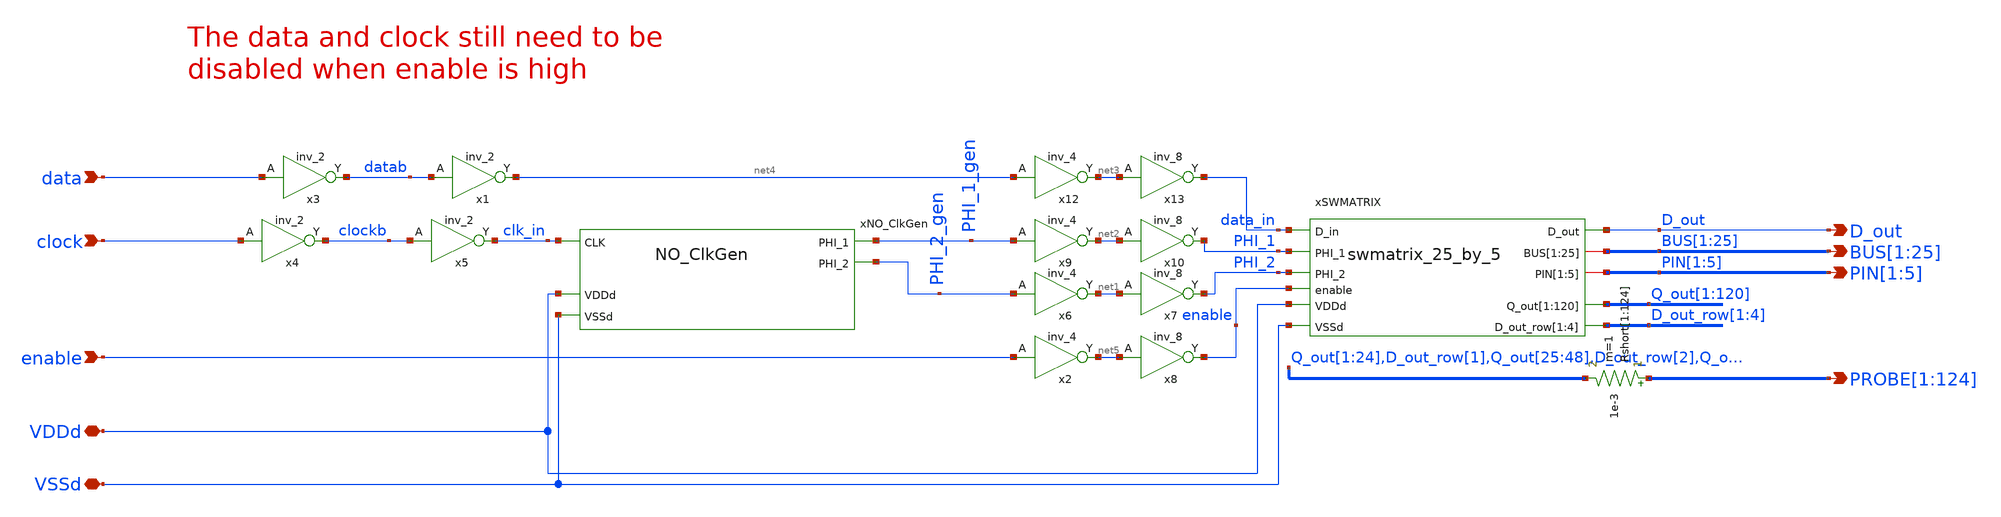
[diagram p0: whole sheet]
** sch_path: full_switch_matrix_25_by_5/full_switch_matrix_25_by_5.sch
**.subckt full_switch_matrix_25_by_5 data clock enable D_out PIN[1],PIN[2],PIN[3],PIN[4],PIN[5]
*+ BUS[1],BUS[2],BUS[3],BUS[4],BUS[5],BUS[6],BUS[7],BUS[8],BUS[9],BUS[10],BUS[11],BUS[12],BUS[13],BUS[14],BUS[15],BUS[16],BUS[17],BUS[18],BUS[19],BUS[20],BUS[21],BUS[22],BUS[23],BUS[24],BUS[25] VSSd VDDd
*+ PROBE[1],PROBE[2],PROBE[3],PROBE[4],PROBE[5],PROBE[6],PROBE[7],PROBE[8],PROBE[9],PROBE[10],PROBE[11],PROBE[12],PROBE[13],PROBE[14],PROBE[15],PROBE[16],PROBE[17],PROBE[18],PROBE[19],PROBE[20],PROBE[21],PROBE[22],PROBE[23],PROBE[24],PROBE[25],PROBE[26],PROBE[27],PROBE[28],PROBE[29],PROBE[30],PROBE[31],PROBE[32],PROBE[33],PROBE[34],PROBE[35],PROBE[36],PROBE[37],PROBE[38],PROBE[39],PROBE[40],PROBE[41],PROBE[42],PROBE[43],PROBE[44],PROBE[45],PROBE[46],PROBE[47],PROBE[48],PROBE[49],PROBE[50],PROBE[51],PROBE[52],PROBE[53],PROBE[54],PROBE[55],PROBE[56],PROBE[57],PROBE[58],PROBE[59],PROBE[60],PROBE[61],PROBE[62],PROBE[63],PROBE[64],PROBE[65],PROBE[66],PROBE[67],PROBE[68],PROBE[69],PROBE[70],PROBE[71],PROBE[72],PROBE[73],PROBE[74],PROBE[75],PROBE[76],PROBE[77],PROBE[78],PROBE[79],PROBE[80],PROBE[81],PROBE[82],PROBE[83],PROBE[84],PROBE[85],PROBE[86],PROBE[87],PROBE[88],PROBE[89],PROBE[90],PROBE[91],PROBE[92],PROBE[93],PROBE[94],PROBE[95],PROBE[96],PROBE[97],PROBE[98],PROBE[99],PROBE[100],PROBE[101],PROBE[102],PROBE[103],PROBE[104],PROBE[105],PROBE[106],PROBE[107],PROBE[108],PROBE[109],PROBE[110],PROBE[111],PROBE[112],PROBE[113],PROBE[114],PROBE[115],PROBE[116],PROBE[117],PROBE[118],PROBE[119],PROBE[120],PROBE[121],PROBE[122],PROBE[123],PROBE[124]
*.ipin data
*.ipin clock
*.ipin enable
*.opin D_out
*.opin PIN[1],PIN[2],PIN[3],PIN[4],PIN[5]
*.opin
*+ BUS[1],BUS[2],BUS[3],BUS[4],BUS[5],BUS[6],BUS[7],BUS[8],BUS[9],BUS[10],BUS[11],BUS[12],BUS[13],BUS[14],BUS[15],BUS[16],BUS[17],BUS[18],BUS[19],BUS[20],BUS[21],BUS[22],BUS[23],BUS[24],BUS[25]
*.iopin VSSd
*.iopin VDDd
*.opin
*+ PROBE[1],PROBE[2],PROBE[3],PROBE[4],PROBE[5],PROBE[6],PROBE[7],PROBE[8],PROBE[9],PROBE[10],PROBE[11],PROBE[12],PROBE[13],PROBE[14],PROBE[15],PROBE[16],PROBE[17],PROBE[18],PROBE[19],PROBE[20],PROBE[21],PROBE[22],PROBE[23],PROBE[24],PROBE[25],PROBE[26],PROBE[27],PROBE[28],PROBE[29],PROBE[30],PROBE[31],PROBE[32],PROBE[33],PROBE[34],PROBE[35],PROBE[36],PROBE[37],PROBE[38],PROBE[39],PROBE[40],PROBE[41],PROBE[42],PROBE[43],PROBE[44],PROBE[45],PROBE[46],PROBE[47],PROBE[48],PROBE[49],PROBE[50],PROBE[51],PROBE[52],PROBE[53],PROBE[54],PROBE[55],PROBE[56],PROBE[57],PROBE[58],PROBE[59],PROBE[60],PROBE[61],PROBE[62],PROBE[63],PROBE[64],PROBE[65],PROBE[66],PROBE[67],PROBE[68],PROBE[69],PROBE[70],PROBE[71],PROBE[72],PROBE[73],PROBE[74],PROBE[75],PROBE[76],PROBE[77],PROBE[78],PROBE[79],PROBE[80],PROBE[81],PROBE[82],PROBE[83],PROBE[84],PROBE[85],PROBE[86],PROBE[87],PROBE[88],PROBE[89],PROBE[90],PROBE[91],PROBE[92],PROBE[93],PROBE[94],PROBE[95],PROBE[96],PROBE[97],PROBE[98],PROBE[99],PROBE[100],PROBE[101],PROBE[102],PROBE[103],PROBE[104],PROBE[105],PROBE[106],PROBE[107],PROBE[108],PROBE[109],PROBE[110],PROBE[111],PROBE[112],PROBE[113],PROBE[114],PROBE[115],PROBE[116],PROBE[117],PROBE[118],PROBE[119],PROBE[120],PROBE[121],PROBE[122],PROBE[123],PROBE[124]
xNO_ClkGen PHI_2_gen clk_in PHI_1_gen VDDd VSSd NO_ClkGen
x3 data VSSd VDDd VSSd VDDd datab gf180mcu_fd_sc_mcu9t5v0__inv_2
x1 datab VSSd VDDd VSSd VDDd net4 gf180mcu_fd_sc_mcu9t5v0__inv_2
x4 clock VSSd VDDd VSSd VDDd clockb gf180mcu_fd_sc_mcu9t5v0__inv_2
x5 clockb VSSd VDDd VSSd VDDd clk_in gf180mcu_fd_sc_mcu9t5v0__inv_2
x6 PHI_2_gen VSSd VDDd VSSd VDDd net1 gf180mcu_fd_sc_mcu9t5v0__inv_4
x7 net1 VSSd VDDd VSSd VDDd PHI_2 gf180mcu_fd_sc_mcu9t5v0__inv_8
x9 PHI_1_gen VSSd VDDd VSSd VDDd net2 gf180mcu_fd_sc_mcu9t5v0__inv_4
x10 net2 VSSd VDDd VSSd VDDd PHI_1 gf180mcu_fd_sc_mcu9t5v0__inv_8
x12 net4 VSSd VDDd VSSd VDDd net3 gf180mcu_fd_sc_mcu9t5v0__inv_4
x13 net3 VSSd VDDd VSSd VDDd data_in gf180mcu_fd_sc_mcu9t5v0__inv_8
x2 enable VSSd VDDd VSSd VDDd net5 gf180mcu_fd_sc_mcu9t5v0__inv_4
x8 net5 VSSd VDDd VSSd VDDd enable gf180mcu_fd_sc_mcu9t5v0__inv_8
xSWMATRIX data_in D_out PHI_1 PHI_2 BUS[1] BUS[2] BUS[3] BUS[4] BUS[5] BUS[6] BUS[7] BUS[8] BUS[9]
+ BUS[10] BUS[11] BUS[12] BUS[13] BUS[14] BUS[15] BUS[16] BUS[17] BUS[18] BUS[19] BUS[20] BUS[21] BUS[22]
+ BUS[23] BUS[24] BUS[25] PIN[1] PIN[2] PIN[3] PIN[4] PIN[5] VDDd VSSd enable Q_out[1] Q_out[2] Q_out[3]
+ Q_out[4] Q_out[5] Q_out[6] Q_out[7] Q_out[8] Q_out[9] Q_out[10] Q_out[11] Q_out[12] Q_out[13] Q_out[14]
+ Q_out[15] Q_out[16] Q_out[17] Q_out[18] Q_out[19] Q_out[20] Q_out[21] Q_out[22] Q_out[23] Q_out[24] Q_out[25]
+ Q_out[26] Q_out[27] Q_out[28] Q_out[29] Q_out[30] Q_out[31] Q_out[32] Q_out[33] Q_out[34] Q_out[35] Q_out[36]
+ Q_out[37] Q_out[38] Q_out[39] Q_out[40] Q_out[41] Q_out[42] Q_out[43] Q_out[44] Q_out[45] Q_out[46] Q_out[47]
+ Q_out[48] Q_out[49] Q_out[50] Q_out[51] Q_out[52] Q_out[53] Q_out[54] Q_out[55] Q_out[56] Q_out[57] Q_out[58]
+ Q_out[59] Q_out[60] Q_out[61] Q_out[62] Q_out[63] Q_out[64] Q_out[65] Q_out[66] Q_out[67] Q_out[68] Q_out[69]
+ Q_out[70] Q_out[71] Q_out[72] Q_out[73] Q_out[74] Q_out[75] Q_out[76] Q_out[77] Q_out[78] Q_out[79] Q_out[80]
+ Q_out[81] Q_out[82] Q_out[83] Q_out[84] Q_out[85] Q_out[86] Q_out[87] Q_out[88] Q_out[89] Q_out[90] Q_out[91]
+ Q_out[92] Q_out[93] Q_out[94] Q_out[95] Q_out[96] Q_out[97] Q_out[98] Q_out[99] Q_out[100] Q_out[101]
+ Q_out[102] Q_out[103] Q_out[104] Q_out[105] Q_out[106] Q_out[107] Q_out[108] Q_out[109] Q_out[110] Q_out[111]
+ Q_out[112] Q_out[113] Q_out[114] Q_out[115] Q_out[116] Q_out[117] Q_out[118] Q_out[119] Q_out[120]
+ D_out_row[1] D_out_row[2] D_out_row[3] D_out_row[4] swmatrix_25_by_5
Rshort[1] PROBE[1] Q_out[1] 1e-3 m=1
Rshort[2] PROBE[2] Q_out[2] 1e-3 m=1
Rshort[3] PROBE[3] Q_out[3] 1e-3 m=1
Rshort[4] PROBE[4] Q_out[4] 1e-3 m=1
Rshort[5] PROBE[5] Q_out[5] 1e-3 m=1
Rshort[6] PROBE[6] Q_out[6] 1e-3 m=1
Rshort[7] PROBE[7] Q_out[7] 1e-3 m=1
Rshort[8] PROBE[8] Q_out[8] 1e-3 m=1
Rshort[9] PROBE[9] Q_out[9] 1e-3 m=1
Rshort[10] PROBE[10] Q_out[10] 1e-3 m=1
Rshort[11] PROBE[11] Q_out[11] 1e-3 m=1
Rshort[12] PROBE[12] Q_out[12] 1e-3 m=1
Rshort[13] PROBE[13] Q_out[13] 1e-3 m=1
Rshort[14] PROBE[14] Q_out[14] 1e-3 m=1
Rshort[15] PROBE[15] Q_out[15] 1e-3 m=1
Rshort[16] PROBE[16] Q_out[16] 1e-3 m=1
Rshort[17] PROBE[17] Q_out[17] 1e-3 m=1
Rshort[18] PROBE[18] Q_out[18] 1e-3 m=1
Rshort[19] PROBE[19] Q_out[19] 1e-3 m=1
Rshort[20] PROBE[20] Q_out[20] 1e-3 m=1
Rshort[21] PROBE[21] Q_out[21] 1e-3 m=1
Rshort[22] PROBE[22] Q_out[22] 1e-3 m=1
Rshort[23] PROBE[23] Q_out[23] 1e-3 m=1
Rshort[24] PROBE[24] Q_out[24] 1e-3 m=1
Rshort[25] PROBE[25] D_out_row[1] 1e-3 m=1
Rshort[26] PROBE[26] Q_out[25] 1e-3 m=1
Rshort[27] PROBE[27] Q_out[26] 1e-3 m=1
Rshort[28] PROBE[28] Q_out[27] 1e-3 m=1
Rshort[29] PROBE[29] Q_out[28] 1e-3 m=1
Rshort[30] PROBE[30] Q_out[29] 1e-3 m=1
Rshort[31] PROBE[31] Q_out[30] 1e-3 m=1
Rshort[32] PROBE[32] Q_out[31] 1e-3 m=1
Rshort[33] PROBE[33] Q_out[32] 1e-3 m=1
Rshort[34] PROBE[34] Q_out[33] 1e-3 m=1
Rshort[35] PROBE[35] Q_out[34] 1e-3 m=1
Rshort[36] PROBE[36] Q_out[35] 1e-3 m=1
Rshort[37] PROBE[37] Q_out[36] 1e-3 m=1
Rshort[38] PROBE[38] Q_out[37] 1e-3 m=1
Rshort[39] PROBE[39] Q_out[38] 1e-3 m=1
Rshort[40] PROBE[40] Q_out[39] 1e-3 m=1
Rshort[41] PROBE[41] Q_out[40] 1e-3 m=1
Rshort[42] PROBE[42] Q_out[41] 1e-3 m=1
Rshort[43] PROBE[43] Q_out[42] 1e-3 m=1
Rshort[44] PROBE[44] Q_out[43] 1e-3 m=1
Rshort[45] PROBE[45] Q_out[44] 1e-3 m=1
Rshort[46] PROBE[46] Q_out[45] 1e-3 m=1
Rshort[47] PROBE[47] Q_out[46] 1e-3 m=1
Rshort[48] PROBE[48] Q_out[47] 1e-3 m=1
Rshort[49] PROBE[49] Q_out[48] 1e-3 m=1
Rshort[50] PROBE[50] D_out_row[2] 1e-3 m=1
Rshort[51] PROBE[51] Q_out[49] 1e-3 m=1
Rshort[52] PROBE[52] Q_out[50] 1e-3 m=1
Rshort[53] PROBE[53] Q_out[51] 1e-3 m=1
Rshort[54] PROBE[54] Q_out[52] 1e-3 m=1
Rshort[55] PROBE[55] Q_out[53] 1e-3 m=1
Rshort[56] PROBE[56] Q_out[54] 1e-3 m=1
Rshort[57] PROBE[57] Q_out[55] 1e-3 m=1
Rshort[58] PROBE[58] Q_out[56] 1e-3 m=1
Rshort[59] PROBE[59] Q_out[57] 1e-3 m=1
Rshort[60] PROBE[60] Q_out[58] 1e-3 m=1
Rshort[61] PROBE[61] Q_out[59] 1e-3 m=1
Rshort[62] PROBE[62] Q_out[60] 1e-3 m=1
Rshort[63] PROBE[63] Q_out[61] 1e-3 m=1
Rshort[64] PROBE[64] Q_out[62] 1e-3 m=1
Rshort[65] PROBE[65] Q_out[63] 1e-3 m=1
Rshort[66] PROBE[66] Q_out[64] 1e-3 m=1
Rshort[67] PROBE[67] Q_out[65] 1e-3 m=1
Rshort[68] PROBE[68] Q_out[66] 1e-3 m=1
Rshort[69] PROBE[69] Q_out[67] 1e-3 m=1
Rshort[70] PROBE[70] Q_out[68] 1e-3 m=1
Rshort[71] PROBE[71] Q_out[69] 1e-3 m=1
Rshort[72] PROBE[72] Q_out[70] 1e-3 m=1
Rshort[73] PROBE[73] Q_out[71] 1e-3 m=1
Rshort[74] PROBE[74] Q_out[72] 1e-3 m=1
Rshort[75] PROBE[75] D_out_row[3] 1e-3 m=1
Rshort[76] PROBE[76] Q_out[73] 1e-3 m=1
Rshort[77] PROBE[77] Q_out[74] 1e-3 m=1
Rshort[78] PROBE[78] Q_out[75] 1e-3 m=1
Rshort[79] PROBE[79] Q_out[76] 1e-3 m=1
Rshort[80] PROBE[80] Q_out[77] 1e-3 m=1
Rshort[81] PROBE[81] Q_out[78] 1e-3 m=1
Rshort[82] PROBE[82] Q_out[79] 1e-3 m=1
Rshort[83] PROBE[83] Q_out[80] 1e-3 m=1
Rshort[84] PROBE[84] Q_out[81] 1e-3 m=1
Rshort[85] PROBE[85] Q_out[82] 1e-3 m=1
Rshort[86] PROBE[86] Q_out[83] 1e-3 m=1
Rshort[87] PROBE[87] Q_out[84] 1e-3 m=1
Rshort[88] PROBE[88] Q_out[85] 1e-3 m=1
Rshort[89] PROBE[89] Q_out[86] 1e-3 m=1
Rshort[90] PROBE[90] Q_out[87] 1e-3 m=1
Rshort[91] PROBE[91] Q_out[88] 1e-3 m=1
Rshort[92] PROBE[92] Q_out[89] 1e-3 m=1
Rshort[93] PROBE[93] Q_out[90] 1e-3 m=1
Rshort[94] PROBE[94] Q_out[91] 1e-3 m=1
Rshort[95] PROBE[95] Q_out[92] 1e-3 m=1
Rshort[96] PROBE[96] Q_out[93] 1e-3 m=1
Rshort[97] PROBE[97] Q_out[94] 1e-3 m=1
Rshort[98] PROBE[98] Q_out[95] 1e-3 m=1
Rshort[99] PROBE[99] Q_out[96] 1e-3 m=1
Rshort[100] PROBE[100] D_out_row[4] 1e-3 m=1
Rshort[101] PROBE[101] Q_out[97] 1e-3 m=1
Rshort[102] PROBE[102] Q_out[98] 1e-3 m=1
Rshort[103] PROBE[103] Q_out[99] 1e-3 m=1
Rshort[104] PROBE[104] Q_out[100] 1e-3 m=1
Rshort[105] PROBE[105] Q_out[101] 1e-3 m=1
Rshort[106] PROBE[106] Q_out[102] 1e-3 m=1
Rshort[107] PROBE[107] Q_out[103] 1e-3 m=1
Rshort[108] PROBE[108] Q_out[104] 1e-3 m=1
Rshort[109] PROBE[109] Q_out[105] 1e-3 m=1
Rshort[110] PROBE[110] Q_out[106] 1e-3 m=1
Rshort[111] PROBE[111] Q_out[107] 1e-3 m=1
Rshort[112] PROBE[112] Q_out[108] 1e-3 m=1
Rshort[113] PROBE[113] Q_out[109] 1e-3 m=1
Rshort[114] PROBE[114] Q_out[110] 1e-3 m=1
Rshort[115] PROBE[115] Q_out[111] 1e-3 m=1
Rshort[116] PROBE[116] Q_out[112] 1e-3 m=1
Rshort[117] PROBE[117] Q_out[113] 1e-3 m=1
Rshort[118] PROBE[118] Q_out[114] 1e-3 m=1
Rshort[119] PROBE[119] Q_out[115] 1e-3 m=1
Rshort[120] PROBE[120] Q_out[116] 1e-3 m=1
Rshort[121] PROBE[121] Q_out[117] 1e-3 m=1
Rshort[122] PROBE[122] Q_out[118] 1e-3 m=1
Rshort[123] PROBE[123] Q_out[119] 1e-3 m=1
Rshort[124] PROBE[124] Q_out[120] 1e-3 m=1
**.ends
.end
